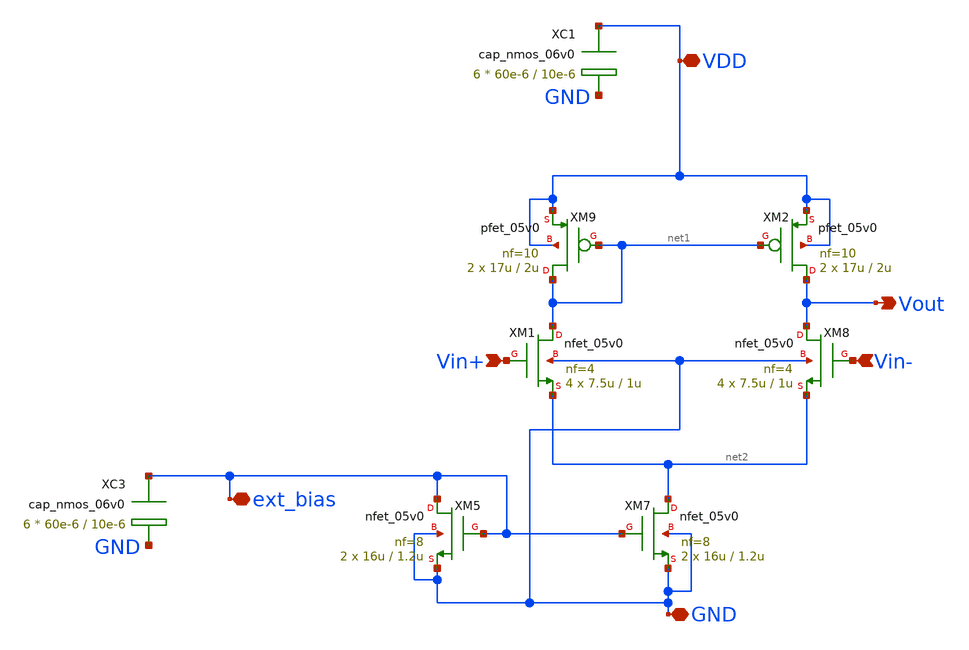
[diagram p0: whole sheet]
** sch_path: MRTMOS_final_chip/gm_ff.sch
**.subckt gm_ff ext_bias Vin+ Vin- GND VDD Vout
*.iopin ext_bias
*.ipin Vin+
*.ipin Vin-
*.iopin GND
*.iopin VDD
*.opin Vout
XC3 ext_bias GND cap_nmos_06v0 c_width=60e-6 c_length=10e-6 m=6
XC1 VDD GND cap_nmos_06v0 c_width=60e-6 c_length=10e-6 m=6
XM7 net2 ext_bias GND GND nfet_05v0 L=1.2u W=16u nf=8 ad='int((nf+1)/2) * W/nf * 0.18u' as='int((nf+2)/2) * W/nf * 0.18u'
+ pd='2*int((nf+1)/2) * (W/nf + 0.18u)' ps='2*int((nf+2)/2) * (W/nf + 0.18u)' nrd='0.18u / W' nrs='0.18u / W'
+ sa=0 sb=0 sd=0 m=2
XM8 Vout Vin- net2 GND nfet_05v0 L=1u W=7.5u nf=4 ad='int((nf+1)/2) * W/nf * 0.18u' as='int((nf+2)/2) * W/nf * 0.18u'
+ pd='2*int((nf+1)/2) * (W/nf + 0.18u)' ps='2*int((nf+2)/2) * (W/nf + 0.18u)' nrd='0.18u / W' nrs='0.18u / W'
+ sa=0 sb=0 sd=0 m=4
XM9 net1 net1 VDD VDD pfet_05v0 L=2u W=17u nf=10 ad='int((nf+1)/2) * W/nf * 0.18u' as='int((nf+2)/2) * W/nf * 0.18u'
+ pd='2*int((nf+1)/2) * (W/nf + 0.18u)' ps='2*int((nf+2)/2) * (W/nf + 0.18u)' nrd='0.18u / W' nrs='0.18u / W'
+ sa=0 sb=0 sd=0 m=2
XM5 ext_bias ext_bias GND GND nfet_05v0 L=1.2u W=16u nf=8 ad='int((nf+1)/2) * W/nf * 0.18u' as='int((nf+2)/2) * W/nf * 0.18u'
+ pd='2*int((nf+1)/2) * (W/nf + 0.18u)' ps='2*int((nf+2)/2) * (W/nf + 0.18u)' nrd='0.18u / W' nrs='0.18u / W'
+ sa=0 sb=0 sd=0 m=2
XM1 net1 Vin+ net2 GND nfet_05v0 L=1u W=7.5u nf=4 ad='int((nf+1)/2) * W/nf * 0.18u' as='int((nf+2)/2) * W/nf * 0.18u'
+ pd='2*int((nf+1)/2) * (W/nf + 0.18u)' ps='2*int((nf+2)/2) * (W/nf + 0.18u)' nrd='0.18u / W' nrs='0.18u / W'
+ sa=0 sb=0 sd=0 m=4
XM2 Vout net1 VDD VDD pfet_05v0 L=2u W=17u nf=10 ad='int((nf+1)/2) * W/nf * 0.18u' as='int((nf+2)/2) * W/nf * 0.18u'
+ pd='2*int((nf+1)/2) * (W/nf + 0.18u)' ps='2*int((nf+2)/2) * (W/nf + 0.18u)' nrd='0.18u / W' nrs='0.18u / W'
+ sa=0 sb=0 sd=0 m=2
**.ends
.end
